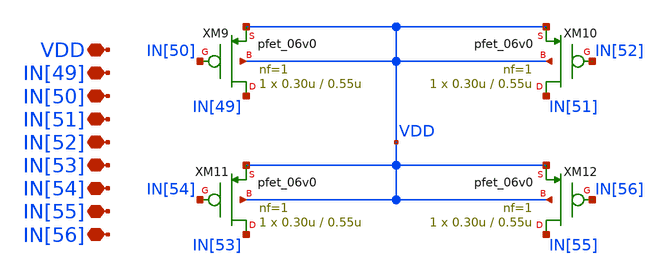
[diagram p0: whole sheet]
** sch_path: designs/libs/core_single-fet/pfet-com/pfet-com.sch
**.subckt pfet-com VDD IN[50] IN[49] IN[51] IN[52] IN[53] IN[54] IN[55] IN[56]
*.iopin VDD
*.iopin IN[50]
*.iopin IN[49]
*.iopin IN[51]
*.iopin IN[52]
*.iopin IN[53]
*.iopin IN[54]
*.iopin IN[55]
*.iopin IN[56]
XM9 IN[49] IN[50] VDD VDD pfet_06v0 L=0.55u W=0.30u nf=1 ad='int((nf+1)/2) * W/nf * 0.18u' as='int((nf+2)/2) * W/nf * 0.18u'
+ pd='2*int((nf+1)/2) * (W/nf + 0.18u)' ps='2*int((nf+2)/2) * (W/nf + 0.18u)' nrd='0.18u / W' nrs='0.18u / W'
+ sa=0 sb=0 sd=0 m=1
XM10 IN[51] IN[52] VDD VDD pfet_06v0 L=0.55u W=0.30u nf=1 ad='int((nf+1)/2) * W/nf * 0.18u' as='int((nf+2)/2) * W/nf * 0.18u'
+ pd='2*int((nf+1)/2) * (W/nf + 0.18u)' ps='2*int((nf+2)/2) * (W/nf + 0.18u)' nrd='0.18u / W' nrs='0.18u / W'
+ sa=0 sb=0 sd=0 m=1
XM11 IN[53] IN[54] VDD VDD pfet_06v0 L=0.55u W=0.30u nf=1 ad='int((nf+1)/2) * W/nf * 0.18u' as='int((nf+2)/2) * W/nf * 0.18u'
+ pd='2*int((nf+1)/2) * (W/nf + 0.18u)' ps='2*int((nf+2)/2) * (W/nf + 0.18u)' nrd='0.18u / W' nrs='0.18u / W'
+ sa=0 sb=0 sd=0 m=1
XM12 IN[55] IN[56] VDD VDD pfet_06v0 L=0.55u W=0.30u nf=1 ad='int((nf+1)/2) * W/nf * 0.18u' as='int((nf+2)/2) * W/nf * 0.18u'
+ pd='2*int((nf+1)/2) * (W/nf + 0.18u)' ps='2*int((nf+2)/2) * (W/nf + 0.18u)' nrd='0.18u / W' nrs='0.18u / W'
+ sa=0 sb=0 sd=0 m=1
**.ends
.end
